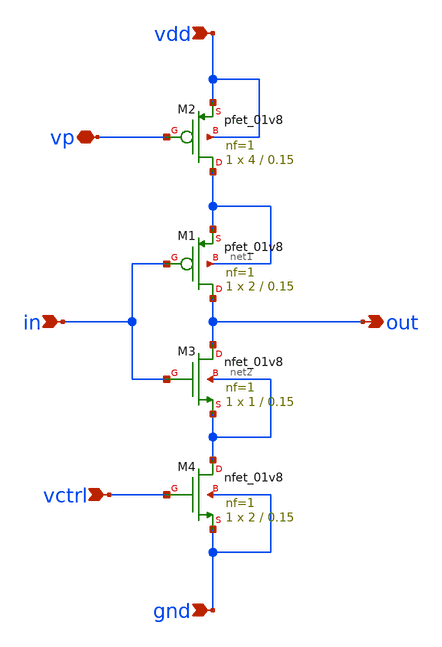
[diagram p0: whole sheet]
** sch_path: vcro/cs_inv.sch
**.subckt cs_inv vctrl in vdd gnd out vp
*.ipin vctrl
*.ipin in
*.ipin vdd
*.ipin gnd
*.opin out
*.iopin vp
XM1 out in net1 net1 sky130_fd_pr__pfet_01v8 L=0.15 W=2 nf=1 ad='int((1 + 1)/2) * 2 / 1 * 0.29' as='int((1 + 2)/2) * 2 / 1 * 0.29'
+ pd='2*int((1 + 1)/2) * (2 / 1 + 0.29)' ps='2*int((1 + 2)/2) * (2 / 1 + 0.29)' nrd='0.29 / 2 ' nrs='0.29 / 2 '
+ sa=0 sb=0 sd=0 mult=1 m=1
XM2 net1 vp vdd vdd sky130_fd_pr__pfet_01v8 L=0.15 W=4 nf=1 ad='int((1 + 1)/2) * 4 / 1 * 0.29' as='int((1 + 2)/2) * 4 / 1 * 0.29'
+ pd='2*int((1 + 1)/2) * (4 / 1 + 0.29)' ps='2*int((1 + 2)/2) * (4 / 1 + 0.29)' nrd='0.29 / 4 ' nrs='0.29 / 4 '
+ sa=0 sb=0 sd=0 mult=1 m=1
XM3 out in net2 net2 sky130_fd_pr__nfet_01v8 L=0.15 W=1 nf=1 ad='int((1 + 1)/2) * 1 / 1 * 0.29' as='int((1 + 2)/2) * 1 / 1 * 0.29'
+ pd='2*int((1 + 1)/2) * (1 / 1 + 0.29)' ps='2*int((1 + 2)/2) * (1 / 1 + 0.29)' nrd='0.29 / 1 ' nrs='0.29 / 1 '
+ sa=0 sb=0 sd=0 mult=1 m=1
XM4 net2 vctrl gnd gnd sky130_fd_pr__nfet_01v8 L=0.15 W=2 nf=1 ad='int((1 + 1)/2) * 2 / 1 * 0.29' as='int((1 + 2)/2) * 2 / 1 * 0.29'
+ pd='2*int((1 + 1)/2) * (2 / 1 + 0.29)' ps='2*int((1 + 2)/2) * (2 / 1 + 0.29)' nrd='0.29 / 2 ' nrs='0.29 / 2 '
+ sa=0 sb=0 sd=0 mult=1 m=1
**.ends
.end
